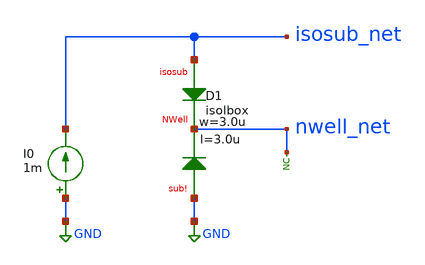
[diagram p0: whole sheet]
** sch_path: ihp-sg13g2/xschem_libs/sg13g2_tests_ase/dc_isolbox/schematic/dc_isolbox.sch
* Copyright 2023 IHP PDK Authors
**.subckt dc_isolbox
I0 GND isosub_net 1m
XD1 isosub_net nwell_net GND isolbox l=3.0u w=3.0u
* noconn nwell_net
**.ends
.GLOBAL GND
.end
